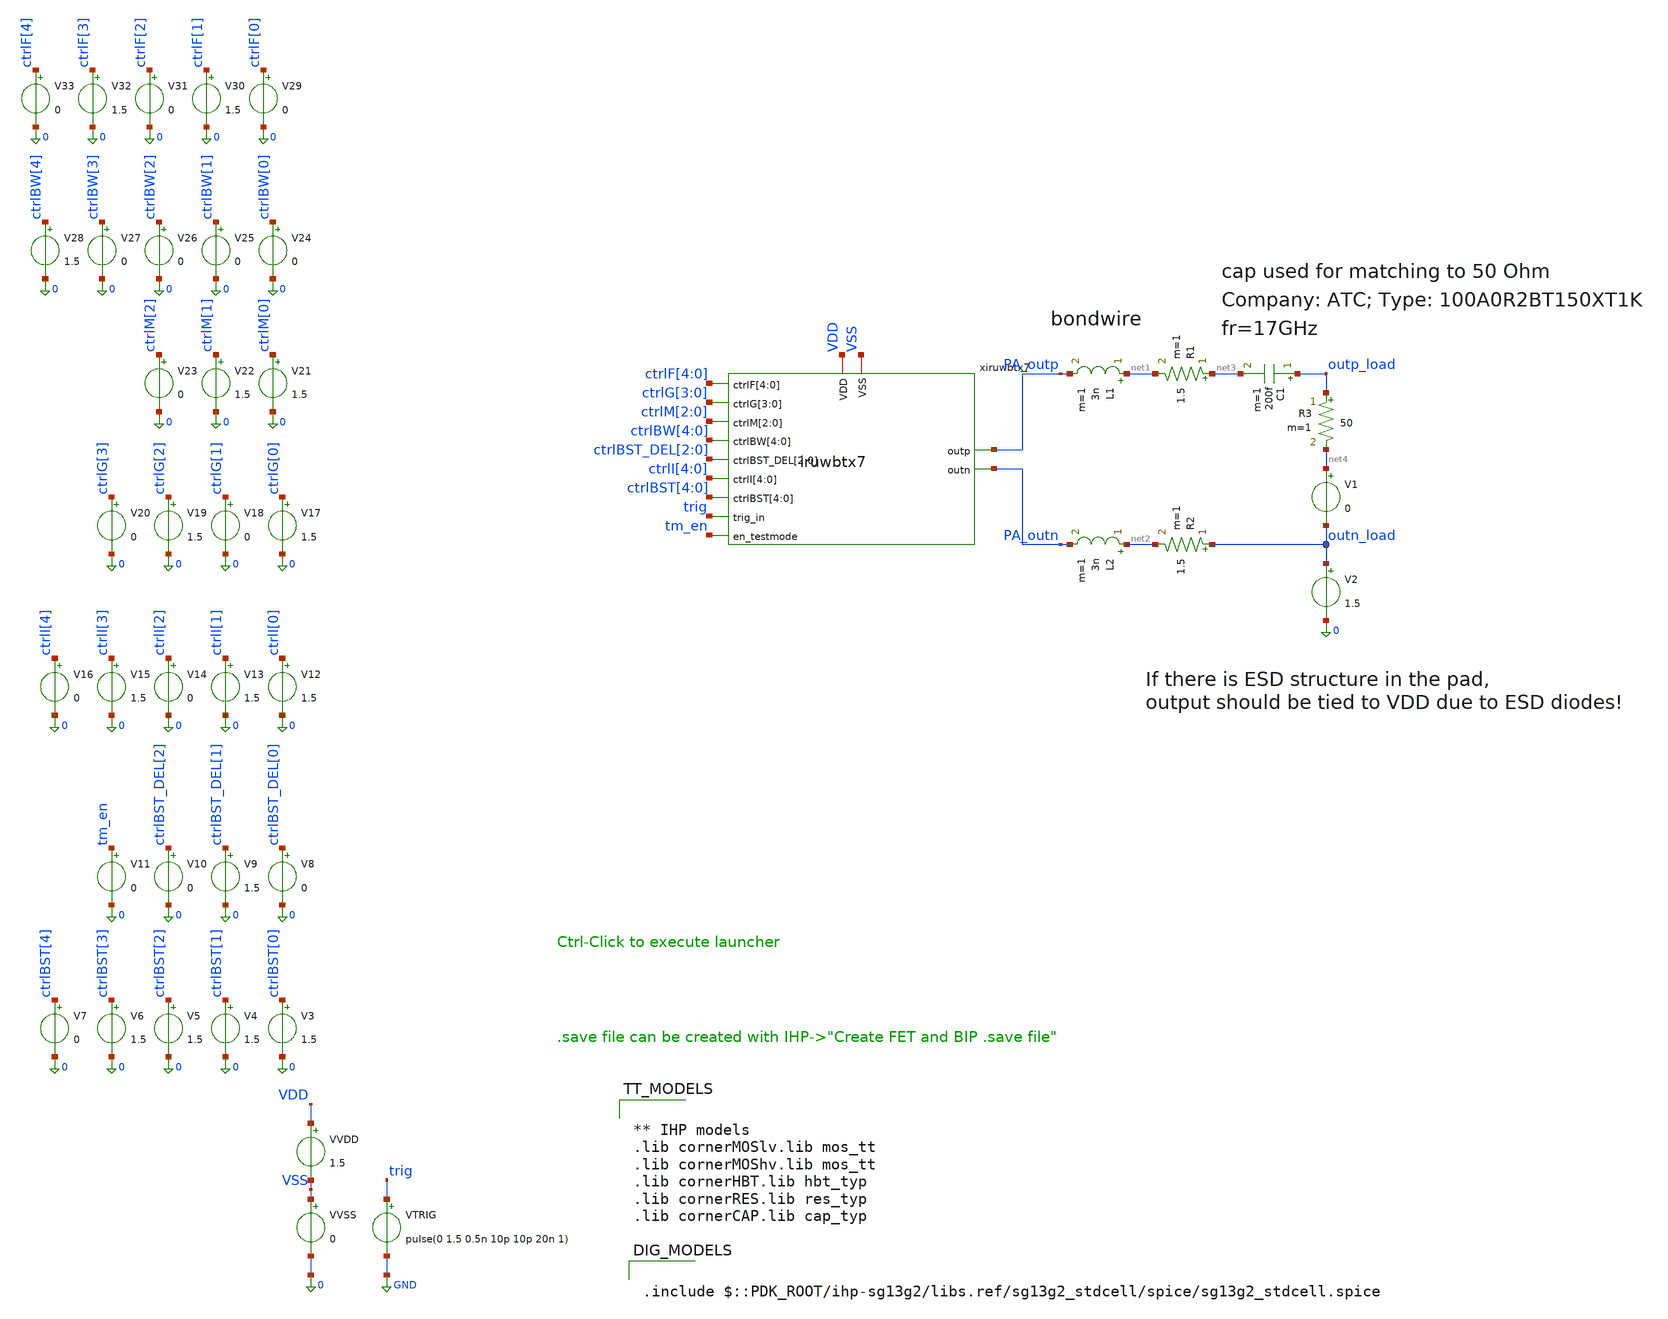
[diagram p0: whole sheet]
** sch_path: xschem/iruwbtx7_tb.sch
* IHP-GmbH/IHP-Open-PDK/ihp-sg13g2/libs.tech/xschem/sg13g2_stdcells/sg13g2_inv_16.sch:
* Copyright 2023 IHP PDK Authors
* Licensed under the Apache License, Version 2.0 (the "License");
**.subckt iruwbtx7_tb
xiruwbtx7 VDD PA_outp PA_outn ctrlF[4] ctrlF[3] ctrlF[2] ctrlF[1] ctrlF[0] ctrlG[3] ctrlG[2]
+ ctrlG[1] ctrlG[0] ctrlM[2] ctrlM[1] ctrlM[0] trig tm_en ctrlBW[4] ctrlBW[3] ctrlBW[2] ctrlBW[1] ctrlBW[0]
+ ctrlBST_DEL[2] ctrlBST_DEL[1] ctrlBST_DEL[0] VSS ctrlI[4] ctrlI[3] ctrlI[2] ctrlI[1] ctrlI[0] ctrlBST[4]
+ ctrlBST[3] ctrlBST[2] ctrlBST[1] ctrlBST[0] iruwbtx7
L1 net1 PA_outp 3n m=1
R1 net3 net1 1.5 m=1
L2 net2 PA_outn 3n m=1
R2 outn_load net2 1.5 m=1
C1 outp_load net3 200f m=1
V1 net4 outn_load 0
R3 outp_load net4 50 m=1
V2 outn_load 0 1.5
VVDD VDD VSS 1.5
VVSS VSS 0 0
VTRIG trig GND pulse(0 1.5 0.5n 10p 10p 20n 1)
V3 ctrlBST[0] 0 1.5
V4 ctrlBST[1] 0 1.5
V5 ctrlBST[2] 0 1.5
V6 ctrlBST[3] 0 1.5
V7 ctrlBST[4] 0 0
V8 ctrlBST_DEL[0] 0 0
V9 ctrlBST_DEL[1] 0 1.5
V10 ctrlBST_DEL[2] 0 0
V11 tm_en 0 0
V12 ctrlI[0] 0 1.5
V13 ctrlI[1] 0 1.5
V14 ctrlI[2] 0 0
V15 ctrlI[3] 0 1.5
V16 ctrlI[4] 0 0
V17 ctrlG[0] 0 1.5
V18 ctrlG[1] 0 0
V19 ctrlG[2] 0 1.5
V20 ctrlG[3] 0 0
V21 ctrlM[0] 0 1.5
V22 ctrlM[1] 0 1.5
V23 ctrlM[2] 0 0
V24 ctrlBW[0] 0 0
V25 ctrlBW[1] 0 0
V26 ctrlBW[2] 0 0
V27 ctrlBW[3] 0 0
V28 ctrlBW[4] 0 1.5
V29 ctrlF[0] 0 0
V30 ctrlF[1] 0 1.5
V31 ctrlF[2] 0 0
V32 ctrlF[3] 0 1.5
V33 ctrlF[4] 0 0
**** begin user architecture code


** IHP models
.lib cornerMOSlv.lib mos_tt
.lib cornerMOShv.lib mos_tt
.lib cornerHBT.lib hbt_typ
.lib cornerRES.lib res_typ
.lib cornerCAP.lib cap_typ





.param temp=27
.include iruwbtx7_tb.save
*.options delmin=10p method=trap reltol=1e-4 vabstol=1e-6 iabstol=1e-12 gmin=1e-12 chgtol=1e-16
*+ rshunt=1e12 trtol=1 pivotrel=1e-3 pivotabs=1e-13 noacct numdgt=7
*.options klu keepopinfo method=Gear rshunt=1e12 gmin=1e-12 reltol=100e-06 abstol=1e-12 vntol=1e-06
*.options method=gear klu reltol=1e-5 vabstol=1e-6 iabstol=1e-12 gmin=1e-12 temp=27 tnom=27
*+ pivrel=1e-3 trtol=2 rshunt=1e12
.options klu method=gear

.control
set num_threads 1

save all
op
write iruwbtx7_tb.raw
set appendwrite
tran 0.5p 6n 0 5p
write iruwbtx7_tb.raw
plot trig
plot xiruwbtx7.VA2 xiruwbtx7.VB2
plot xiruwbtx7.en_PA
plot xiruwbtx7.rf_osci_p xiruwbtx7.rf_osci_n
plot outp_load outn_load
.endc





.include $::PDK_ROOT/ihp-sg13g2/libs.ref/sg13g2_stdcell/spice/sg13g2_stdcell.spice


**** end user architecture code
**.ends

* expanding   symbol:  iruwbtx7.sym # of pins=13
** sym_path: xschem/iruwbtx7.sym
** sch_path: xschem/iruwbtx7.sch
.subckt iruwbtx7 VDD outp outn ctrlF[4] ctrlF[3] ctrlF[2] ctrlF[1] ctrlF[0] ctrlG[3] ctrlG[2]
+ ctrlG[1] ctrlG[0] ctrlM[2] ctrlM[1] ctrlM[0] trig_in en_testmode ctrlBW[4] ctrlBW[3] ctrlBW[2] ctrlBW[1]
+ ctrlBW[0] ctrlBST_DEL[2] ctrlBST_DEL[1] ctrlBST_DEL[0] VSS ctrlI[4] ctrlI[3] ctrlI[2] ctrlI[1] ctrlI[0]
+ ctrlBST[4] ctrlBST[3] ctrlBST[2] ctrlBST[1] ctrlBST[0]
*.ipin ctrlF[4],ctrlF[3],ctrlF[2],ctrlF[1],ctrlF[0]
*.iopin VDD
*.ipin trig_in
*.ipin en_testmode
*.ipin ctrlBW[4],ctrlBW[3],ctrlBW[2],ctrlBW[1],ctrlBW[0]
*.ipin ctrlBST_DEL[2],ctrlBST_DEL[1],ctrlBST_DEL[0]
*.ipin ctrlI[4],ctrlI[3],ctrlI[2],ctrlI[1],ctrlI[0]
*.ipin ctrlBST[4],ctrlBST[3],ctrlBST[2],ctrlBST[1],ctrlBST[0]
*.iopin VSS
*.opin outp
*.opin outn
*.ipin ctrlG[3],ctrlG[2],ctrlG[1],ctrlG[0]
*.ipin ctrlM[2],ctrlM[1],ctrlM[0]
xosci_capBank rf_osci_n rf_osci_p ctrlF[4] ctrlF[3] ctrlF[2] ctrlF[1] ctrlF[0] VSS
+ iruwbtx7_osci_capBank
xosci_core rf_osci_n rf_osci_p VA4 VA3 VA2 VA1 VA0 VB4 VB3 VB2 VB1 VB0 VSS iruwbtx7_osci_core
xosci_decoder ctrlBW[4] ctrlBW[3] ctrlBW[2] ctrlBW[1] ctrlBW[0] ctrlBST_DEL[2] ctrlBST_DEL[1]
+ ctrlBST_DEL[0] ctrlI[4] ctrlI[3] ctrlI[2] ctrlI[1] ctrlI[0] VDD VSS ctrlBST[4] ctrlBST[3] ctrlBST[2] ctrlBST[1]
+ ctrlBST[0] en_testmode VA4 VA3 VA2 VA1 VA0 trig_in VB4 VB3 VB2 VB1 VB0 en_PA iruwbtx7_osci_decoder
xtank_inductor VDD rf_osci_n rf_osci_p iruwbtx7_tank_inductor
xPA outn outp VDD ctrlM[2] ctrlM[1] ctrlM[0] rf_osci_n VSS rf_osci_p ctrlG[3] ctrlG[2] ctrlG[1]
+ ctrlG[0] en_PA iruwbtx7_PA
.ends


* expanding   symbol:  iruwbtx7_osci_capBank.sym # of pins=4
** sym_path: xschem/iruwbtx7_osci_capBank.sym
** sch_path: xschem/iruwbtx7_osci_capBank.sch
.subckt iruwbtx7_osci_capBank rf_n rf_p ctrlF[4] ctrlF[3] ctrlF[2] ctrlF[1] ctrlF[0] VSS
*.ipin ctrlF[4],ctrlF[3],ctrlF[2],ctrlF[1],ctrlF[0]
*.iopin VSS
*.iopin rf_p
*.iopin rf_n
XC1[15] rf_n net1 VSS cap_rfcmim w=7.0e-6 l=7.0e-6 wfeed=1.0e-6 m=1 mm_ok=1
XC1[14] rf_n net1 VSS cap_rfcmim w=7.0e-6 l=7.0e-6 wfeed=1.0e-6 m=1 mm_ok=1
XC1[13] rf_n net1 VSS cap_rfcmim w=7.0e-6 l=7.0e-6 wfeed=1.0e-6 m=1 mm_ok=1
XC1[12] rf_n net1 VSS cap_rfcmim w=7.0e-6 l=7.0e-6 wfeed=1.0e-6 m=1 mm_ok=1
XC1[11] rf_n net1 VSS cap_rfcmim w=7.0e-6 l=7.0e-6 wfeed=1.0e-6 m=1 mm_ok=1
XC1[10] rf_n net1 VSS cap_rfcmim w=7.0e-6 l=7.0e-6 wfeed=1.0e-6 m=1 mm_ok=1
XC1[9] rf_n net1 VSS cap_rfcmim w=7.0e-6 l=7.0e-6 wfeed=1.0e-6 m=1 mm_ok=1
XC1[8] rf_n net1 VSS cap_rfcmim w=7.0e-6 l=7.0e-6 wfeed=1.0e-6 m=1 mm_ok=1
XC1[7] rf_n net1 VSS cap_rfcmim w=7.0e-6 l=7.0e-6 wfeed=1.0e-6 m=1 mm_ok=1
XC1[6] rf_n net1 VSS cap_rfcmim w=7.0e-6 l=7.0e-6 wfeed=1.0e-6 m=1 mm_ok=1
XC1[5] rf_n net1 VSS cap_rfcmim w=7.0e-6 l=7.0e-6 wfeed=1.0e-6 m=1 mm_ok=1
XC1[4] rf_n net1 VSS cap_rfcmim w=7.0e-6 l=7.0e-6 wfeed=1.0e-6 m=1 mm_ok=1
XC1[3] rf_n net1 VSS cap_rfcmim w=7.0e-6 l=7.0e-6 wfeed=1.0e-6 m=1 mm_ok=1
XC1[2] rf_n net1 VSS cap_rfcmim w=7.0e-6 l=7.0e-6 wfeed=1.0e-6 m=1 mm_ok=1
XC1[1] rf_n net1 VSS cap_rfcmim w=7.0e-6 l=7.0e-6 wfeed=1.0e-6 m=1 mm_ok=1
XC1[0] rf_n net1 VSS cap_rfcmim w=7.0e-6 l=7.0e-6 wfeed=1.0e-6 m=1 mm_ok=1
XM1 net1 ctrlF[4] VSS VSS sg13_lv_nmos w=10.0u l=0.13u ng=1 m=16 rfmode=1 mm_ok=1
XM2 net2 ctrlF[4] VSS VSS sg13_lv_nmos w=10.0u l=0.13u ng=1 m=16 rfmode=1 mm_ok=1
XM3 net1 ctrlF[4] net2 VSS sg13_lv_nmos w=10.0u l=0.13u ng=1 m=32 rfmode=1 mm_ok=1
XC2[15] rf_p net2 VSS cap_rfcmim w=7.0e-6 l=7.0e-6 wfeed=1.0e-6 m=1 mm_ok=1
XC2[14] rf_p net2 VSS cap_rfcmim w=7.0e-6 l=7.0e-6 wfeed=1.0e-6 m=1 mm_ok=1
XC2[13] rf_p net2 VSS cap_rfcmim w=7.0e-6 l=7.0e-6 wfeed=1.0e-6 m=1 mm_ok=1
XC2[12] rf_p net2 VSS cap_rfcmim w=7.0e-6 l=7.0e-6 wfeed=1.0e-6 m=1 mm_ok=1
XC2[11] rf_p net2 VSS cap_rfcmim w=7.0e-6 l=7.0e-6 wfeed=1.0e-6 m=1 mm_ok=1
XC2[10] rf_p net2 VSS cap_rfcmim w=7.0e-6 l=7.0e-6 wfeed=1.0e-6 m=1 mm_ok=1
XC2[9] rf_p net2 VSS cap_rfcmim w=7.0e-6 l=7.0e-6 wfeed=1.0e-6 m=1 mm_ok=1
XC2[8] rf_p net2 VSS cap_rfcmim w=7.0e-6 l=7.0e-6 wfeed=1.0e-6 m=1 mm_ok=1
XC2[7] rf_p net2 VSS cap_rfcmim w=7.0e-6 l=7.0e-6 wfeed=1.0e-6 m=1 mm_ok=1
XC2[6] rf_p net2 VSS cap_rfcmim w=7.0e-6 l=7.0e-6 wfeed=1.0e-6 m=1 mm_ok=1
XC2[5] rf_p net2 VSS cap_rfcmim w=7.0e-6 l=7.0e-6 wfeed=1.0e-6 m=1 mm_ok=1
XC2[4] rf_p net2 VSS cap_rfcmim w=7.0e-6 l=7.0e-6 wfeed=1.0e-6 m=1 mm_ok=1
XC2[3] rf_p net2 VSS cap_rfcmim w=7.0e-6 l=7.0e-6 wfeed=1.0e-6 m=1 mm_ok=1
XC2[2] rf_p net2 VSS cap_rfcmim w=7.0e-6 l=7.0e-6 wfeed=1.0e-6 m=1 mm_ok=1
XC2[1] rf_p net2 VSS cap_rfcmim w=7.0e-6 l=7.0e-6 wfeed=1.0e-6 m=1 mm_ok=1
XC2[0] rf_p net2 VSS cap_rfcmim w=7.0e-6 l=7.0e-6 wfeed=1.0e-6 m=1 mm_ok=1
XC3[7] rf_n net3 VSS cap_rfcmim w=7.0e-6 l=7.0e-6 wfeed=1.0e-6 m=1 mm_ok=1
XC3[6] rf_n net3 VSS cap_rfcmim w=7.0e-6 l=7.0e-6 wfeed=1.0e-6 m=1 mm_ok=1
XC3[5] rf_n net3 VSS cap_rfcmim w=7.0e-6 l=7.0e-6 wfeed=1.0e-6 m=1 mm_ok=1
XC3[4] rf_n net3 VSS cap_rfcmim w=7.0e-6 l=7.0e-6 wfeed=1.0e-6 m=1 mm_ok=1
XC3[3] rf_n net3 VSS cap_rfcmim w=7.0e-6 l=7.0e-6 wfeed=1.0e-6 m=1 mm_ok=1
XC3[2] rf_n net3 VSS cap_rfcmim w=7.0e-6 l=7.0e-6 wfeed=1.0e-6 m=1 mm_ok=1
XC3[1] rf_n net3 VSS cap_rfcmim w=7.0e-6 l=7.0e-6 wfeed=1.0e-6 m=1 mm_ok=1
XC3[0] rf_n net3 VSS cap_rfcmim w=7.0e-6 l=7.0e-6 wfeed=1.0e-6 m=1 mm_ok=1
XM4 net3 ctrlF[3] VSS VSS sg13_lv_nmos w=10.0u l=0.13u ng=1 m=8 rfmode=1 mm_ok=1
XM5 net4 ctrlF[3] VSS VSS sg13_lv_nmos w=10.0u l=0.13u ng=1 m=8 rfmode=1 mm_ok=1
XM6 net3 ctrlF[3] net4 VSS sg13_lv_nmos w=10.0u l=0.13u ng=1 m=16 rfmode=1 mm_ok=1
XC4[7] rf_p net4 VSS cap_rfcmim w=7.0e-6 l=7.0e-6 wfeed=1.0e-6 m=1 mm_ok=1
XC4[6] rf_p net4 VSS cap_rfcmim w=7.0e-6 l=7.0e-6 wfeed=1.0e-6 m=1 mm_ok=1
XC4[5] rf_p net4 VSS cap_rfcmim w=7.0e-6 l=7.0e-6 wfeed=1.0e-6 m=1 mm_ok=1
XC4[4] rf_p net4 VSS cap_rfcmim w=7.0e-6 l=7.0e-6 wfeed=1.0e-6 m=1 mm_ok=1
XC4[3] rf_p net4 VSS cap_rfcmim w=7.0e-6 l=7.0e-6 wfeed=1.0e-6 m=1 mm_ok=1
XC4[2] rf_p net4 VSS cap_rfcmim w=7.0e-6 l=7.0e-6 wfeed=1.0e-6 m=1 mm_ok=1
XC4[1] rf_p net4 VSS cap_rfcmim w=7.0e-6 l=7.0e-6 wfeed=1.0e-6 m=1 mm_ok=1
XC4[0] rf_p net4 VSS cap_rfcmim w=7.0e-6 l=7.0e-6 wfeed=1.0e-6 m=1 mm_ok=1
XC5[3] rf_n net5 VSS cap_rfcmim w=7.0e-6 l=7.0e-6 wfeed=1.0e-6 m=1 mm_ok=1
XC5[2] rf_n net5 VSS cap_rfcmim w=7.0e-6 l=7.0e-6 wfeed=1.0e-6 m=1 mm_ok=1
XC5[1] rf_n net5 VSS cap_rfcmim w=7.0e-6 l=7.0e-6 wfeed=1.0e-6 m=1 mm_ok=1
XC5[0] rf_n net5 VSS cap_rfcmim w=7.0e-6 l=7.0e-6 wfeed=1.0e-6 m=1 mm_ok=1
XM7 net5 ctrlF[2] VSS VSS sg13_lv_nmos w=10.0u l=0.13u ng=1 m=4 rfmode=1 mm_ok=1
XM8 net6 ctrlF[2] VSS VSS sg13_lv_nmos w=10.0u l=0.13u ng=1 m=4 rfmode=1 mm_ok=1
XM9 net5 ctrlF[2] net6 VSS sg13_lv_nmos w=10.0u l=0.13u ng=1 m=8 rfmode=1 mm_ok=1
XC6[3] rf_p net6 VSS cap_rfcmim w=7.0e-6 l=7.0e-6 wfeed=1.0e-6 m=1 mm_ok=1
XC6[2] rf_p net6 VSS cap_rfcmim w=7.0e-6 l=7.0e-6 wfeed=1.0e-6 m=1 mm_ok=1
XC6[1] rf_p net6 VSS cap_rfcmim w=7.0e-6 l=7.0e-6 wfeed=1.0e-6 m=1 mm_ok=1
XC6[0] rf_p net6 VSS cap_rfcmim w=7.0e-6 l=7.0e-6 wfeed=1.0e-6 m=1 mm_ok=1
XC7[1] rf_n net7 VSS cap_rfcmim w=7.0e-6 l=7.0e-6 wfeed=1.0e-6 m=1 mm_ok=1
XC7[0] rf_n net7 VSS cap_rfcmim w=7.0e-6 l=7.0e-6 wfeed=1.0e-6 m=1 mm_ok=1
XM10 net7 ctrlF[1] VSS VSS sg13_lv_nmos w=10.0u l=0.13u ng=1 m=2 rfmode=1 mm_ok=1
XM11 net8 ctrlF[1] VSS VSS sg13_lv_nmos w=10.0u l=0.13u ng=1 m=2 rfmode=1 mm_ok=1
XM12 net7 ctrlF[1] net8 VSS sg13_lv_nmos w=10.0u l=0.13u ng=1 m=4 rfmode=1 mm_ok=1
XC8[1] rf_p net8 VSS cap_rfcmim w=7.0e-6 l=7.0e-6 wfeed=1.0e-6 m=1 mm_ok=1
XC8[0] rf_p net8 VSS cap_rfcmim w=7.0e-6 l=7.0e-6 wfeed=1.0e-6 m=1 mm_ok=1
XC9 rf_n net9 VSS cap_rfcmim w=7.0e-6 l=7.0e-6 wfeed=1.0e-6 m=1 mm_ok=1
XM13 net9 ctrlF[0] VSS VSS sg13_lv_nmos w=10.0u l=0.13u ng=1 m=1 rfmode=1 mm_ok=1
XM14 net10 ctrlF[0] VSS VSS sg13_lv_nmos w=10.0u l=0.13u ng=1 m=1 rfmode=1 mm_ok=1
XM15 net9 ctrlF[0] net10 VSS sg13_lv_nmos w=10.0u l=0.13u ng=1 m=2 rfmode=1 mm_ok=1
XC10 rf_p net10 VSS cap_rfcmim w=7.0e-6 l=7.0e-6 wfeed=1.0e-6 m=1 mm_ok=1
.ends


* expanding   symbol:  iruwbtx7_osci_core.sym # of pins=5
** sym_path: xschem/iruwbtx7_osci_core.sym
** sch_path: xschem/iruwbtx7_osci_core.sch
.subckt iruwbtx7_osci_core rf_n rf_p VA[4] VA[3] VA[2] VA[1] VA[0] VB[4] VB[3] VB[2] VB[1] VB[0] VSS
*.iopin rf_p
*.iopin rf_n
*.ipin VA[4],VA[3],VA[2],VA[1],VA[0]
*.ipin VB[4],VB[3],VB[2],VB[1],VB[0]
*.iopin VSS
XM1 net1 VA[0] VSS VSS sg13_lv_nmos w=2.5u l=0.13u ng=1 m=1 mm_ok=1
XM2 net1 VA[1] VSS VSS sg13_lv_nmos w=2.5u l=0.13u ng=1 m=2 mm_ok=1
XM3 net1 VA[2] VSS VSS sg13_lv_nmos w=2.5u l=0.13u ng=1 m=4 mm_ok=1
XM4 net1 VA[3] VSS VSS sg13_lv_nmos w=2.5u l=0.13u ng=1 m=8 mm_ok=1
XM5 net1 VA[4] VSS VSS sg13_lv_nmos w=2.5u l=0.13u ng=1 m=16 mm_ok=1
XM6 net2 VB[0] VSS VSS sg13_lv_nmos w=2.5u l=0.13u ng=1 m=1 mm_ok=1
XM7 net2 VB[1] VSS VSS sg13_lv_nmos w=2.5u l=0.13u ng=1 m=2 mm_ok=1
XM8 net2 VB[2] VSS VSS sg13_lv_nmos w=2.5u l=0.13u ng=1 m=4 mm_ok=1
XM9 net2 VB[3] VSS VSS sg13_lv_nmos w=2.5u l=0.13u ng=1 m=8 mm_ok=1
XM10 net2 VB[4] VSS VSS sg13_lv_nmos w=2.5u l=0.13u ng=1 m=16 mm_ok=1
XC1 net1 net2 VSS cap_rfcmim w=18.195e-6 l=18.195e-6 wfeed=3.0e-6 m=1 mm_ok=1
XC2 net2 net1 VSS cap_rfcmim w=18.195e-6 l=18.195e-6 wfeed=3.0e-6 m=1 mm_ok=1
XM11 rf_n rf_p net2 VSS sg13_hv_nmos w=100u l=0.45u ng=10 m=3 rfmode=1 mm_ok=1
XM12 rf_p rf_n net1 VSS sg13_hv_nmos w=100u l=0.45u ng=10 m=3 rfmode=1 mm_ok=1
.ends


* expanding   symbol:  iruwbtx7_osci_decoder.sym # of pins=11
** sym_path: xschem/iruwbtx7_osci_decoder.sym
** sch_path: xschem/iruwbtx7_osci_decoder.sch
.subckt iruwbtx7_osci_decoder ctrlBW[4] ctrlBW[3] ctrlBW[2] ctrlBW[1] ctrlBW[0] ctrlBST_DEL[2]
+ ctrlBST_DEL[1] ctrlBST_DEL[0] ctrlI[4] ctrlI[3] ctrlI[2] ctrlI[1] ctrlI[0] VDD VSS ctrlBST[4] ctrlBST[3]
+ ctrlBST[2] ctrlBST[1] ctrlBST[0] en_testmode VA[4] VA[3] VA[2] VA[1] VA[0] trig_in VB[4] VB[3] VB[2] VB[1]
+ VB[0] en_PA
*.ipin en_testmode
*.ipin trig_in
*.ipin ctrlBW[4],ctrlBW[3],ctrlBW[2],ctrlBW[1],ctrlBW[0]
*.iopin VDD
*.iopin VSS
*.ipin ctrlBST_DEL[2],ctrlBST_DEL[1],ctrlBST_DEL[0]
*.ipin ctrlI[4],ctrlI[3],ctrlI[2],ctrlI[1],ctrlI[0]
*.ipin ctrlBST[4],ctrlBST[3],ctrlBST[2],ctrlBST[1],ctrlBST[0]
*.opin VA[4],VA[3],VA[2],VA[1],VA[0]
*.opin VB[4],VB[3],VB[2],VB[1],VB[0]
*.opin en_PA
x1 net3 en_testmode trig_in VDD VSS sg13g2_nand2_1
x2 net1 trig_in VDD VSS sg13g2_inv_1
x3 net4 net1 VDD VSS sg13g2_inv_2
x4 net2 trig_in VDD VSS sg13g2_inv_1
x5 net5 net2 VDD VSS sg13g2_inv_1
XC5 net5 net6 cap_cmim w=7.0e-6 l=7.0e-6 m=1 mm_ok=1
XM1 net6 ctrlBW[0] VSS VSS sg13_lv_nmos w=1u l=0.13u ng=1 m=1 mm_ok=1
XC1 net5 net7 cap_cmim w=7.0e-6 l=7.0e-6 m=2 mm_ok=1
XM2 net7 ctrlBW[1] VSS VSS sg13_lv_nmos w=1u l=0.13u ng=1 m=2 mm_ok=1
XC2 net5 net8 cap_cmim w=7.0e-6 l=7.0e-6 m=4 mm_ok=1
XM3 net8 ctrlBW[2] VSS VSS sg13_lv_nmos w=1u l=0.13u ng=1 m=4 mm_ok=1
XC3 net5 net9 cap_cmim w=7.0e-6 l=7.0e-6 m=8 mm_ok=1
XM4 net9 ctrlBW[3] VSS VSS sg13_lv_nmos w=1u l=0.13u ng=1 m=8 mm_ok=1
XC4 net5 net10 cap_cmim w=7.0e-6 l=7.0e-6 m=16 mm_ok=1
XM5 net10 ctrlBW[4] VSS VSS sg13_lv_nmos w=1u l=0.13u ng=1 m=16 mm_ok=1
x6 net12 net5 VDD VSS sg13g2_inv_1
x7 net11 net12 VDD VSS sg13g2_inv_2
x8 net14 net11 VDD VSS sg13g2_inv_2
x9 net13 net4 net14 VDD VSS sg13g2_nand2_2
x10 net15 net3 net13 VDD VSS sg13g2_nand2_2
x11 net24 net15 VDD VSS sg13g2_inv_2
x12 net16 trig_in VDD VSS sg13g2_inv_1
x13 net17 net16 VDD VSS sg13g2_inv_1
x14 net22 net17 VDD VSS sg13g2_inv_1
x15 net21 net22 VDD VSS sg13g2_inv_2
x16 net23 net21 VDD VSS sg13g2_inv_2
x17 net40 net4 net23 VDD VSS sg13g2_nand2_2
XM6 net17 ctrlBST_DEL[0] net18 VSS sg13_lv_nmos w=1u l=0.13u ng=1 m=1 mm_ok=1
XM7 net17 ctrlBST_DEL[1] net19 VSS sg13_lv_nmos w=1u l=0.13u ng=1 m=2 mm_ok=1
XM11 net17 ctrlBST_DEL[2] net20 VSS sg13_lv_nmos w=1u l=0.13u ng=1 m=4 mm_ok=1
XM8 VSS net18 VSS VSS sg13_lv_nmos w=0.6u l=1.0u ng=1 m=1 mm_ok=1
XM9 VSS net19 VSS VSS sg13_lv_nmos w=0.6u l=1.0u ng=1 m=2 mm_ok=1
XM10 VSS net20 VSS VSS sg13_lv_nmos w=0.6u l=1.0u ng=1 m=4 mm_ok=1
x18 net25 net24 VDD VSS sg13g2_inv_1
x19 net27 net25 VDD VSS sg13g2_inv_1
x20 net26 net27 VDD VSS sg13g2_inv_1
x21 net34 net26 VDD VSS sg13g2_inv_1
x22 net29 net24 VDD VSS sg13g2_inv_1
x23 net28 net29 VDD VSS sg13g2_inv_1
x24 net63 net28 VDD VSS sg13g2_inv_4
x25 net31 net34 VDD VSS sg13g2_inv_1
x26 net30 net31 VDD VSS sg13g2_inv_1
x27 net36 net30 VDD VSS sg13g2_inv_4
x28 net33 net24 VDD VSS sg13g2_inv_1
x29 net32 net33 VDD VSS sg13g2_inv_1
x30 net35 net32 VDD VSS sg13g2_inv_4
x31 net37 net40 VDD VSS sg13g2_inv_1
x32 net39 net37 VDD VSS sg13g2_inv_1
x33 net38 net39 VDD VSS sg13g2_inv_1
x34 net45 net38 VDD VSS sg13g2_inv_1
x35 net42 net45 VDD VSS sg13g2_inv_1
x36 net41 net42 VDD VSS sg13g2_inv_1
x37 net51 net41 VDD VSS sg13g2_inv_4
x38 net44 net40 VDD VSS sg13g2_inv_1
x39 net43 net44 VDD VSS sg13g2_inv_1
x40 net50 net43 VDD VSS sg13g2_inv_4
x41[4] net46[4] ctrlI[4] net35 VDD VSS sg13g2_nand2_2
x41[3] net46[3] ctrlI[3] net35 VDD VSS sg13g2_nand2_2
x41[2] net46[2] ctrlI[2] net35 VDD VSS sg13g2_nand2_2
x41[1] net46[1] ctrlI[1] net35 VDD VSS sg13g2_nand2_2
x41[0] net46[0] ctrlI[0] net35 VDD VSS sg13g2_nand2_2
x1[4] net47[4] net46[4] VDD VSS sg13g2_inv_2
x1[3] net47[3] net46[3] VDD VSS sg13g2_inv_2
x1[2] net47[2] net46[2] VDD VSS sg13g2_inv_2
x1[1] net47[1] net46[1] VDD VSS sg13g2_inv_2
x1[0] net47[0] net46[0] VDD VSS sg13g2_inv_2
x2[4] net48[4] net36 ctrlI[4] VDD VSS sg13g2_nand2_2
x2[3] net48[3] net36 ctrlI[3] VDD VSS sg13g2_nand2_2
x2[2] net48[2] net36 ctrlI[2] VDD VSS sg13g2_nand2_2
x2[1] net48[1] net36 ctrlI[1] VDD VSS sg13g2_nand2_2
x2[0] net48[0] net36 ctrlI[0] VDD VSS sg13g2_nand2_2
x3[4] net49[4] net48[4] VDD VSS sg13g2_inv_2
x3[3] net49[3] net48[3] VDD VSS sg13g2_inv_2
x3[2] net49[2] net48[2] VDD VSS sg13g2_inv_2
x3[1] net49[1] net48[1] VDD VSS sg13g2_inv_2
x3[0] net49[0] net48[0] VDD VSS sg13g2_inv_2
x4[4] net52[4] ctrlBST[4] net50 VDD VSS sg13g2_nand2_2
x4[3] net52[3] ctrlBST[3] net50 VDD VSS sg13g2_nand2_2
x4[2] net52[2] ctrlBST[2] net50 VDD VSS sg13g2_nand2_2
x4[1] net52[1] ctrlBST[1] net50 VDD VSS sg13g2_nand2_2
x4[0] net52[0] ctrlBST[0] net50 VDD VSS sg13g2_nand2_2
x5[4] net54[4] net52[4] VDD VSS sg13g2_inv_2
x5[3] net54[3] net52[3] VDD VSS sg13g2_inv_2
x5[2] net54[2] net52[2] VDD VSS sg13g2_inv_2
x5[1] net54[1] net52[1] VDD VSS sg13g2_inv_2
x5[0] net54[0] net52[0] VDD VSS sg13g2_inv_2
x6[4] net53[4] net51 ctrlBST[4] VDD VSS sg13g2_nand2_2
x6[3] net53[3] net51 ctrlBST[3] VDD VSS sg13g2_nand2_2
x6[2] net53[2] net51 ctrlBST[2] VDD VSS sg13g2_nand2_2
x6[1] net53[1] net51 ctrlBST[1] VDD VSS sg13g2_nand2_2
x6[0] net53[0] net51 ctrlBST[0] VDD VSS sg13g2_nand2_2
x7[4] net55[4] net53[4] VDD VSS sg13g2_inv_2
x7[3] net55[3] net53[3] VDD VSS sg13g2_inv_2
x7[2] net55[2] net53[2] VDD VSS sg13g2_inv_2
x7[1] net55[1] net53[1] VDD VSS sg13g2_inv_2
x7[0] net55[0] net53[0] VDD VSS sg13g2_inv_2
x8[4] net56[4] net54[4] net47[4] VDD VSS sg13g2_nor2_2
x8[3] net56[3] net54[3] net47[3] VDD VSS sg13g2_nor2_2
x8[2] net56[2] net54[2] net47[2] VDD VSS sg13g2_nor2_2
x8[1] net56[1] net54[1] net47[1] VDD VSS sg13g2_nor2_2
x8[0] net56[0] net54[0] net47[0] VDD VSS sg13g2_nor2_2
x42[4] net59[4] net49[4] net55[4] VDD VSS sg13g2_nor2_2
x42[3] net59[3] net49[3] net55[3] VDD VSS sg13g2_nor2_2
x42[2] net59[2] net49[2] net55[2] VDD VSS sg13g2_nor2_2
x42[1] net59[1] net49[1] net55[1] VDD VSS sg13g2_nor2_2
x42[0] net59[0] net49[0] net55[0] VDD VSS sg13g2_nor2_2
x9[4] net57[4] net56[4] VDD VSS sg13g2_inv_4
x9[3] net57[3] net56[3] VDD VSS sg13g2_inv_4
x9[2] net57[2] net56[2] VDD VSS sg13g2_inv_4
x9[1] net57[1] net56[1] VDD VSS sg13g2_inv_4
x9[0] net57[0] net56[0] VDD VSS sg13g2_inv_4
x10[4] net58[4] net57[4] VDD VSS sg13g2_inv_8
x10[3] net58[3] net57[3] VDD VSS sg13g2_inv_8
x10[2] net58[2] net57[2] VDD VSS sg13g2_inv_8
x10[1] net58[1] net57[1] VDD VSS sg13g2_inv_8
x10[0] net58[0] net57[0] VDD VSS sg13g2_inv_8
x11[4] VA[4] net58[4] VDD VSS sg13g2_inv_16
x11[3] VA[3] net58[3] VDD VSS sg13g2_inv_16
x11[2] VA[2] net58[2] VDD VSS sg13g2_inv_16
x11[1] VA[1] net58[1] VDD VSS sg13g2_inv_16
x11[0] VA[0] net58[0] VDD VSS sg13g2_inv_16
x12[4] net60[4] net59[4] VDD VSS sg13g2_inv_4
x12[3] net60[3] net59[3] VDD VSS sg13g2_inv_4
x12[2] net60[2] net59[2] VDD VSS sg13g2_inv_4
x12[1] net60[1] net59[1] VDD VSS sg13g2_inv_4
x12[0] net60[0] net59[0] VDD VSS sg13g2_inv_4
x13[4] net61[4] net60[4] VDD VSS sg13g2_inv_8
x13[3] net61[3] net60[3] VDD VSS sg13g2_inv_8
x13[2] net61[2] net60[2] VDD VSS sg13g2_inv_8
x13[1] net61[1] net60[1] VDD VSS sg13g2_inv_8
x13[0] net61[0] net60[0] VDD VSS sg13g2_inv_8
x14[4] VB[4] net61[4] VDD VSS sg13g2_inv_16
x14[3] VB[3] net61[3] VDD VSS sg13g2_inv_16
x14[2] VB[2] net61[2] VDD VSS sg13g2_inv_16
x14[1] VB[1] net61[1] VDD VSS sg13g2_inv_16
x14[0] VB[0] net61[0] VDD VSS sg13g2_inv_16
x15[4] net62[4] net63 VDD VSS sg13g2_inv_8
x15[3] net62[3] net63 VDD VSS sg13g2_inv_8
x15[2] net62[2] net63 VDD VSS sg13g2_inv_8
x15[1] net62[1] net63 VDD VSS sg13g2_inv_8
x15[0] net62[0] net63 VDD VSS sg13g2_inv_8
x16[4] en_PA net62[4] VDD VSS sg13g2_inv_16
x16[3] en_PA net62[3] VDD VSS sg13g2_inv_16
x16[2] en_PA net62[2] VDD VSS sg13g2_inv_16
x16[1] en_PA net62[1] VDD VSS sg13g2_inv_16
x16[0] en_PA net62[0] VDD VSS sg13g2_inv_16
* noconn VDD
.ends


* expanding   symbol:  iruwbtx7_tank_inductor.sym # of pins=3
** sym_path: xschem/iruwbtx7_tank_inductor.sym
** sch_path: xschem/iruwbtx7_tank_inductor.sch
.subckt iruwbtx7_tank_inductor LC LB LA
*.iopin LC
*.iopin LA
*.iopin LB
L1 LC net2 200p m=1
L2 net1 LC 200p m=1
R1 net2 LA 1.65 m=1
R2 LB net1 1.65 m=1
.ends


* expanding   symbol:  iruwbtx7_PA.sym # of pins=9
** sym_path: xschem/iruwbtx7_PA.sym
** sch_path: xschem/iruwbtx7_PA.sch
.subckt iruwbtx7_PA outn outp VDD ctrlM[2] ctrlM[1] ctrlM[0] inn VSS inp ctrlG[3] ctrlG[2] ctrlG[1]
+ ctrlG[0] en_PA
*.iopin VDD
*.opin outn
*.opin outp
*.ipin ctrlM[2],ctrlM[1],ctrlM[0]
*.ipin inp
*.ipin inn
*.iopin VSS
*.ipin ctrlG[3],ctrlG[2],ctrlG[1],ctrlG[0]
*.ipin en_PA
xbalun outn outp VDD rf_p rf_n iruwbtx7_balun
XC2 outn VSS VSS cap_rfcmim w=25.105e-6 l=25.105e-6 wfeed=3.0e-6 m=1 mm_ok=1
XC1 outp VSS VSS cap_rfcmim w=25.105e-6 l=25.105e-6 wfeed=3.0e-6 m=1 mm_ok=1
xPA_capBank rf_n rf_p ctrlM[2] ctrlM[1] ctrlM[0] VSS iruwbtx7_PA_capBank
xPA_currentMirror VDD net2[3] net2[2] net2[1] net2[0] net1 en_PA VSS iruwbtx7_PA_currentMirror
xPA_decoder VDD VSS ctrlG[3] ctrlG[2] ctrlG[1] ctrlG[0] net2[3] net2[2] net2[1] net2[0] en_PA
+ iruwbtx7_PA_decoder
XM2 rf_n inp net1 VSS sg13_lv_nmos w=100u l=0.45u ng=10 m=3 mm_ok=1
XM1 rf_p inn net1 VSS sg13_lv_nmos w=100u l=0.45u ng=10 m=3 mm_ok=1
.ends


* expanding   symbol:  sg13g2_nand2_1.sym # of pins=3
** sym_path: sg13g2_nand2_1.sym
** sch_path: sg13g2_nand2_1.sch
.subckt sg13g2_nand2_1 Y A B VDD VSS
*.iopin VDD
*.iopin VSS
*.ipin A
*.ipin B
*.opin Y
XM1 Y A net1 VSS sg13_lv_nmos w=740.00n l=130.00n ng=1 m=1 mm_ok=1
XM2 net1 B VSS VSS sg13_lv_nmos w=740.00n l=130.00n ng=1 m=1 mm_ok=1
XM3 Y A VDD VDD sg13_lv_pmos w=1.12u l=130.00n ng=1 m=1 mm_ok=1
XM4 Y B VDD VDD sg13_lv_pmos w=1.12u l=130.00n ng=1 m=1 mm_ok=1
.ends


* expanding   symbol:  sg13g2_inv_1.sym # of pins=2
** sym_path: sg13g2_inv_1.sym
** sch_path: sg13g2_inv_1.sch
.subckt sg13g2_inv_1 Y A VDD VSS
*.opin Y
*.ipin A
*.iopin VDD
*.iopin VSS
XM1 Y A VSS VSS sg13_lv_nmos w=740.00n l=130.00n ng=1 m=1 mm_ok=1
XM2 Y A VDD VDD sg13_lv_pmos w=1.12u l=130.00n ng=1 m=1 mm_ok=1
.ends


* expanding   symbol:  sg13g2_inv_2.sym # of pins=2
** sym_path: sg13g2_inv_2.sym
** sch_path: sg13g2_inv_2.sch
.subckt sg13g2_inv_2 Y A VDD VSS
*.opin Y
*.ipin A
*.iopin VDD
*.iopin VSS
XM1 Y A VSS VSS sg13_lv_nmos w=1.48u l=130.00n ng=2 m=1 mm_ok=1
XM2 Y A VDD VDD sg13_lv_pmos w=2.24u l=130.00n ng=2 m=1 mm_ok=1
.ends


* expanding   symbol:  sg13g2_nand2_2.sym # of pins=3
** sym_path: sg13g2_nand2_2.sym
** sch_path: sg13g2_nand2_2.sch
.subckt sg13g2_nand2_2 Y A B VDD VSS
*.iopin VDD
*.iopin VSS
*.opin Y
*.ipin B
*.ipin A
XM1 Y A net1 VSS sg13_lv_nmos w=1.44u l=130.00n ng=2 m=1 mm_ok=1
XM2 net1 B VSS VSS sg13_lv_nmos w=1.44u l=130.00n ng=2 m=1 mm_ok=1
XM3 Y A VDD VDD sg13_lv_pmos w=2.24u l=130.00n ng=2 m=1 mm_ok=1
XM4 Y B VDD VDD sg13_lv_pmos w=2.24u l=130.00n ng=2 m=1 mm_ok=1
.ends


* expanding   symbol:  sg13g2_inv_4.sym # of pins=2
** sym_path: sg13g2_inv_4.sym
** sch_path: sg13g2_inv_4.sch
.subckt sg13g2_inv_4 Y A VDD VSS
*.ipin A
*.opin Y
*.iopin VDD
*.iopin VSS
XM1 Y A VSS VSS sg13_lv_nmos w=2.96u l=130.00n ng=4 m=1 mm_ok=1
XM2 Y A VDD VDD sg13_lv_pmos w=4.48u l=130.00n ng=4 m=1 mm_ok=1
.ends


* expanding   symbol:  sg13g2_nor2_2.sym # of pins=3
** sym_path: sg13g2_nor2_2.sym
** sch_path: sg13g2_nor2_2.sch
.subckt sg13g2_nor2_2 Y A B VDD VSS
*.opin Y
*.ipin B
*.ipin A
*.iopin VDD
*.iopin VSS
XM1 Y A VSS VSS sg13_lv_nmos w=1.48u l=130.00n ng=2 m=1 mm_ok=1
XM2 Y B VSS VSS sg13_lv_nmos w=1.48u l=130.00n ng=2 m=1 mm_ok=1
XM3 net1 A VDD VDD sg13_lv_pmos w=2.24u l=130.00n ng=2 m=1 mm_ok=1
XM4 Y B net1 VDD sg13_lv_pmos w=2.24u l=130.00n ng=2 m=1 mm_ok=1
.ends


* expanding   symbol:  sg13g2_inv_8.sym # of pins=2
** sym_path: sg13g2_inv_8.sym
** sch_path: sg13g2_inv_8.sch
.subckt sg13g2_inv_8 Y A VDD VSS
*.opin Y
*.ipin A
*.iopin VDD
*.iopin VSS
XM1 Y A VSS VSS sg13_lv_nmos w=5.92u l=130.00n ng=8 m=1 mm_ok=1
XM2 Y A VDD VDD sg13_lv_pmos w=8.96u l=130.00n ng=8 m=1 mm_ok=1
.ends


* expanding   symbol:  sg13g2_inv_16.sym # of pins=2
** sym_path: sg13g2_inv_16.sym
** sch_path: sg13g2_inv_16.sch
.subckt sg13g2_inv_16 Y A VDD VSS
*.opin Y
*.iopin VSS
*.ipin A
*.iopin VDD
XM1 Y A VSS VSS sg13_lv_nmos w=11.84u l=130.00n ng=16 m=1 mm_ok=1
XM2 Y A VDD VDD sg13_lv_pmos w=17.92u l=130.00n ng=16 m=1 mm_ok=1
.ends


* expanding   symbol:  iruwbtx7_balun.sym # of pins=5
** sym_path: xschem/iruwbtx7_balun.sym
** sch_path: xschem/iruwbtx7_balun.sch
.subckt iruwbtx7_balun LD LE LC LB LA
*.iopin LC
*.iopin LA
*.iopin LB
*.iopin LD
*.iopin LE
L1 LC net2 411p m=1
L2 net1 LC 411p m=1
R1 net2 LA 2.18 m=1
R2 LB net1 2.18 m=1
L3 net3 net5 483p m=1
L4 net4 net3 483p m=1
R3 net5 LD 3.6 m=1
R4 LE net4 3.6 m=1
K1 L1 L3 0.74
K2 L2 L4 0.74
.ends


* expanding   symbol:  iruwbtx7_PA_capBank.sym # of pins=4
** sym_path: xschem/iruwbtx7_PA_capBank.sym
** sch_path: xschem/iruwbtx7_PA_capBank.sch
.subckt iruwbtx7_PA_capBank rf_n rf_p ctrlM[2] ctrlM[1] ctrlM[0] VSS
*.ipin ctrlM[2],ctrlM[1],ctrlM[0]
*.iopin VSS
*.iopin rf_p
*.iopin rf_n
XC5[3] rf_n net1 VSS cap_rfcmim w=7.0e-6 l=7.0e-6 wfeed=1.0e-6 m=1 mm_ok=1
XC5[2] rf_n net1 VSS cap_rfcmim w=7.0e-6 l=7.0e-6 wfeed=1.0e-6 m=1 mm_ok=1
XC5[1] rf_n net1 VSS cap_rfcmim w=7.0e-6 l=7.0e-6 wfeed=1.0e-6 m=1 mm_ok=1
XC5[0] rf_n net1 VSS cap_rfcmim w=7.0e-6 l=7.0e-6 wfeed=1.0e-6 m=1 mm_ok=1
XM7 net1 ctrlM[2] VSS VSS sg13_lv_nmos w=10.0u l=0.13u ng=1 m=4 rfmode=1 mm_ok=1
XM8 net2 ctrlM[2] VSS VSS sg13_lv_nmos w=10.0u l=0.13u ng=1 m=4 rfmode=1 mm_ok=1
XM9 net1 ctrlM[2] net2 VSS sg13_lv_nmos w=10.0u l=0.13u ng=1 m=8 rfmode=1 mm_ok=1
XC6[3] rf_p net2 VSS cap_rfcmim w=7.0e-6 l=7.0e-6 wfeed=1.0e-6 m=1 mm_ok=1
XC6[2] rf_p net2 VSS cap_rfcmim w=7.0e-6 l=7.0e-6 wfeed=1.0e-6 m=1 mm_ok=1
XC6[1] rf_p net2 VSS cap_rfcmim w=7.0e-6 l=7.0e-6 wfeed=1.0e-6 m=1 mm_ok=1
XC6[0] rf_p net2 VSS cap_rfcmim w=7.0e-6 l=7.0e-6 wfeed=1.0e-6 m=1 mm_ok=1
XC7[1] rf_n net3 VSS cap_rfcmim w=7.0e-6 l=7.0e-6 wfeed=1.0e-6 m=1 mm_ok=1
XC7[0] rf_n net3 VSS cap_rfcmim w=7.0e-6 l=7.0e-6 wfeed=1.0e-6 m=1 mm_ok=1
XM10 net3 ctrlM[1] VSS VSS sg13_lv_nmos w=10.0u l=0.13u ng=1 m=2 rfmode=1 mm_ok=1
XM11 net4 ctrlM[1] VSS VSS sg13_lv_nmos w=10.0u l=0.13u ng=1 m=2 rfmode=1 mm_ok=1
XM12 net3 ctrlM[1] net4 VSS sg13_lv_nmos w=10.0u l=0.13u ng=1 m=4 rfmode=1 mm_ok=1
XC8[1] rf_p net4 VSS cap_rfcmim w=7.0e-6 l=7.0e-6 wfeed=1.0e-6 m=1 mm_ok=1
XC8[0] rf_p net4 VSS cap_rfcmim w=7.0e-6 l=7.0e-6 wfeed=1.0e-6 m=1 mm_ok=1
XC9 rf_n net5 VSS cap_rfcmim w=7.0e-6 l=7.0e-6 wfeed=1.0e-6 m=1 mm_ok=1
XM13 net5 ctrlM[0] VSS VSS sg13_lv_nmos w=10.0u l=0.13u ng=1 m=1 rfmode=1 mm_ok=1
XM14 net6 ctrlM[0] VSS VSS sg13_lv_nmos w=10.0u l=0.13u ng=1 m=1 rfmode=1 mm_ok=1
XM15 net5 ctrlM[0] net6 VSS sg13_lv_nmos w=10.0u l=0.13u ng=1 m=2 rfmode=1 mm_ok=1
XC10 rf_p net6 VSS cap_rfcmim w=7.0e-6 l=7.0e-6 wfeed=1.0e-6 m=1 mm_ok=1
.ends


* expanding   symbol:  iruwbtx7_PA_currentMirror.sym # of pins=5
** sym_path: xschem/iruwbtx7_PA_currentMirror.sym
** sch_path: xschem/iruwbtx7_PA_currentMirror.sch
.subckt iruwbtx7_PA_currentMirror VDD en_G[3] en_G[2] en_G[1] en_G[0] ibias en_ref VSS
*.iopin ibias
*.ipin en_ref
*.iopin VSS
*.iopin VDD
*.ipin en_G[3],en_G[2],en_G[1],en_G[0]
XM1 ibias net2 net1 VSS sg13_lv_nmos w=80.0u l=0.5u ng=10 m=2 mm_ok=1
XM2 net1 en_G[0] VSS VSS sg13_lv_nmos w=30.0u l=0.13u ng=10 m=2 mm_ok=1
XM3 ibias net2 net3 VSS sg13_lv_nmos w=80.0u l=0.5u ng=10 m=4 mm_ok=1
XM4 net3 en_G[1] VSS VSS sg13_lv_nmos w=30.0u l=0.13u ng=10 m=4 mm_ok=1
XM5 ibias net2 net4 VSS sg13_lv_nmos w=80.0u l=0.5u ng=10 m=8 mm_ok=1
XM6 net4 en_G[2] VSS VSS sg13_lv_nmos w=30.0u l=0.13u ng=10 m=8 mm_ok=1
XM7 ibias net2 net5 VSS sg13_lv_nmos w=80.0u l=0.5u ng=10 m=16 mm_ok=1
XM8 net5 en_G[3] VSS VSS sg13_lv_nmos w=30.0u l=0.13u ng=10 m=16 mm_ok=1
XM9 net2 net2 net6 VSS sg13_lv_nmos w=80.0u l=0.5u ng=10 m=1 mm_ok=1
XM10 net6 en_ref VSS VSS sg13_lv_nmos w=30.0u l=0.13u ng=10 m=1 mm_ok=1
XR1 VDD net2 VSS rppd w=1.7e-6 l=6.3e-6 m=1 b=0 mm_ok=1
.ends


* expanding   symbol:  iruwbtx7_PA_decoder.sym # of pins=5
** sym_path: xschem/iruwbtx7_PA_decoder.sym
** sch_path: xschem/iruwbtx7_PA_decoder.sch
.subckt iruwbtx7_PA_decoder VDD VSS ctrlG[3] ctrlG[2] ctrlG[1] ctrlG[0] en_out[3] en_out[2]
+ en_out[1] en_out[0] en_in
*.ipin ctrlG[3],ctrlG[2],ctrlG[1],ctrlG[0]
*.ipin en_in
*.opin en_out[3],en_out[2],en_out[1],en_out[0]
*.iopin VDD
*.iopin VSS
x10[3] net3[3] ctrlG[3] en_in VDD VSS sg13g2_nand2_2
x10[2] net3[2] ctrlG[2] en_in VDD VSS sg13g2_nand2_2
x10[1] net3[1] ctrlG[1] en_in VDD VSS sg13g2_nand2_2
x10[0] net3[0] ctrlG[0] en_in VDD VSS sg13g2_nand2_2
x9[3] net1[3] net3[3] VDD VSS sg13g2_inv_2
x9[2] net1[2] net3[2] VDD VSS sg13g2_inv_2
x9[1] net1[1] net3[1] VDD VSS sg13g2_inv_2
x9[0] net1[0] net3[0] VDD VSS sg13g2_inv_2
x1[3] net2[3] net1[3] VDD VSS sg13g2_inv_8
x1[2] net2[2] net1[2] VDD VSS sg13g2_inv_8
x1[1] net2[1] net1[1] VDD VSS sg13g2_inv_8
x1[0] net2[0] net1[0] VDD VSS sg13g2_inv_8
x11[3] en_out[3] net2[3] VDD VSS sg13g2_inv_16
x11[2] en_out[2] net2[2] VDD VSS sg13g2_inv_16
x11[1] en_out[1] net2[1] VDD VSS sg13g2_inv_16
x11[0] en_out[0] net2[0] VDD VSS sg13g2_inv_16
.ends

.GLOBAL GND
.end
